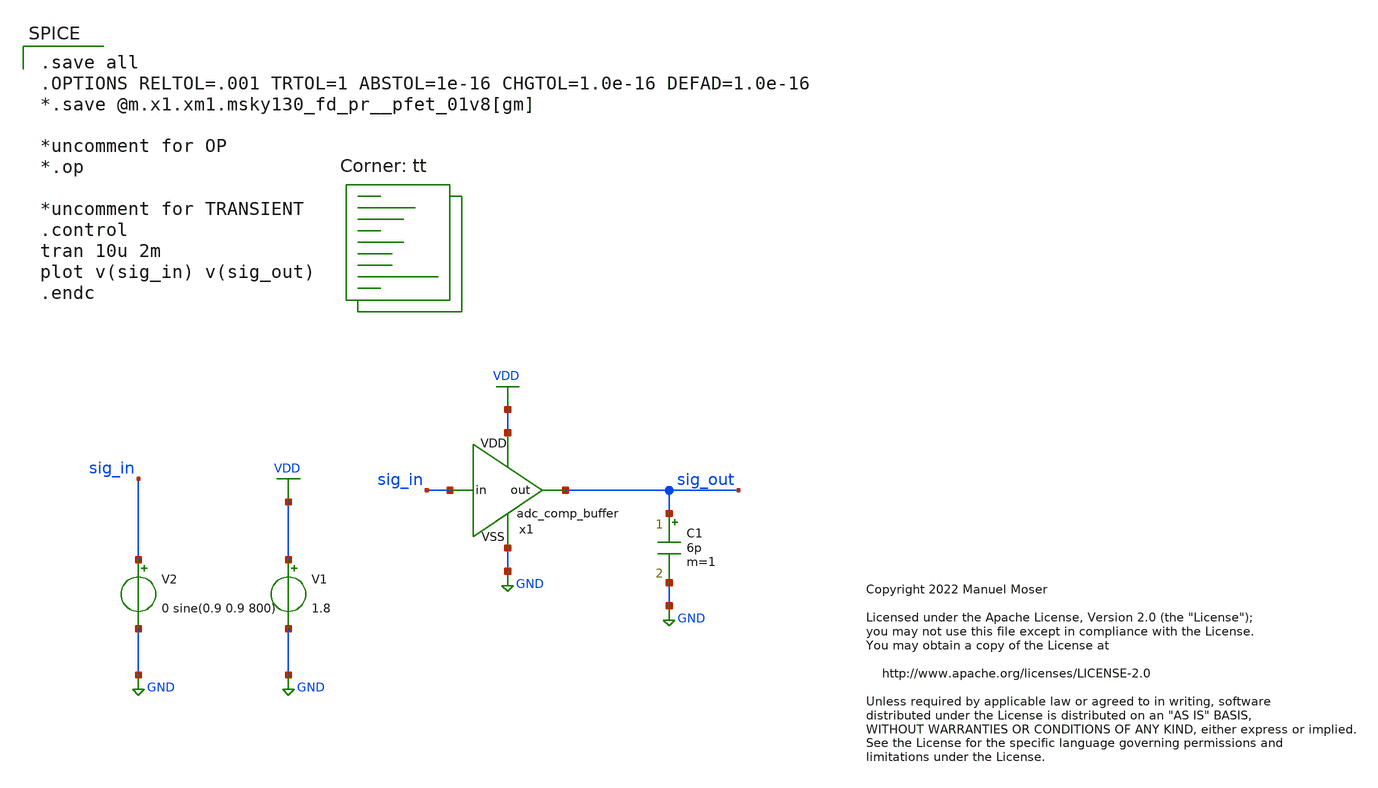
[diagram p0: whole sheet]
** sch_path: xschem/adc_comp_buffer/adc_comp_buffer_tb.sch
* Copyright 2022 Manuel Moser
* Licensed under the Apache License, Version 2.0 (the "License");
**.subckt adc_comp_buffer_tb
V1 VDD GND 1.8
V2 sig_in GND 0 sine(0.9 0.9 800)
C1 sig_out GND 6p m=1
x1 VDD GND sig_in sig_out adc_comp_buffer
**** begin user architecture code

.save all
.OPTIONS RELTOL=.001 TRTOL=1 ABSTOL=1e-16 CHGTOL=1.0e-16 DEFAD=1.0e-16
*.save @m.x1.xm1.msky130_fd_pr__pfet_01v8[gm]

*uncomment for OP
*.op

*uncomment for TRANSIENT
.control
tran 10u 2m
plot v(sig_in) v(sig_out)
.endc


.lib $::SKYWATER_MODELS/sky130.lib.spice tt
**** end user architecture code
**.ends

* expanding   symbol:  adc_comp_buffer.sym # of pins=4
** sym_path: xschem/adc_comp_buffer.sym
** sch_path: xschem/adc_comp_buffer.sch
.subckt adc_comp_buffer VDD VSS in out
*.iopin VDD
*.iopin VSS
*.ipin in
*.opin out
XM5 net1 in VSS VSS sky130_fd_pr__nfet_01v8 L=0.15 W=0.5 nf=1 ad='int((nf+1)/2) * W/nf * 0.29' as='int((nf+2)/2) * W/nf * 0.29'
+ pd='2*int((nf+1)/2) * (W/nf + 0.29)' ps='2*int((nf+2)/2) * (W/nf + 0.29)' nrd='0.29 / W' nrs='0.29 / W'
+ sa=0 sb=0 sd=0 mult=1 m=1
XM1 net1 in VDD VDD sky130_fd_pr__pfet_01v8 L=0.15 W=1 nf=1 ad='int((nf+1)/2) * W/nf * 0.29' as='int((nf+2)/2) * W/nf * 0.29'
+ pd='2*int((nf+1)/2) * (W/nf + 0.29)' ps='2*int((nf+2)/2) * (W/nf + 0.29)' nrd='0.29 / W' nrs='0.29 / W'
+ sa=0 sb=0 sd=0 mult=1 m=1
XM2 out net1 VDD VDD sky130_fd_pr__pfet_01v8 L=0.15 W=2 nf=2 ad='int((nf+1)/2) * W/nf * 0.29' as='int((nf+2)/2) * W/nf * 0.29'
+ pd='2*int((nf+1)/2) * (W/nf + 0.29)' ps='2*int((nf+2)/2) * (W/nf + 0.29)' nrd='0.29 / W' nrs='0.29 / W'
+ sa=0 sb=0 sd=0 mult=1 m=1
XM6 out net1 VSS VSS sky130_fd_pr__nfet_01v8 L=0.15 W=1 nf=2 ad='int((nf+1)/2) * W/nf * 0.29' as='int((nf+2)/2) * W/nf * 0.29'
+ pd='2*int((nf+1)/2) * (W/nf + 0.29)' ps='2*int((nf+2)/2) * (W/nf + 0.29)' nrd='0.29 / W' nrs='0.29 / W'
+ sa=0 sb=0 sd=0 mult=1 m=1
.ends

.GLOBAL GND
.GLOBAL VDD
.end
